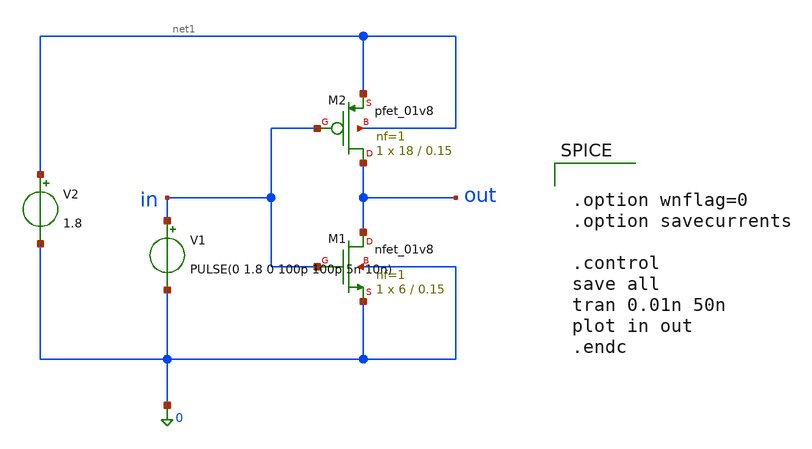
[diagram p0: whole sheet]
** sch_path: inverter_transient.sch
**.subckt inverter_transient
XM1 out in 0 0 sky130_fd_pr__nfet_01v8 L=0.15 W=6 nf=1 ad='int((1 + 1)/2) * 6 / 1 * 0.29' as='int((1 + 2)/2) * 6 / 1 * 0.29'
+ pd='2*int((1 + 1)/2) * (6 / 1 + 0.29)' ps='2*int((1 + 2)/2) * (6 / 1 + 0.29)' nrd='0.29 / 6 ' nrs='0.29 / 6 '
+ sa=0 sb=0 sd=0 mult=1 m=1
XM2 out in net1 net1 sky130_fd_pr__pfet_01v8 L=0.15 W=18 nf=1 ad='int((1 + 1)/2) * 18 / 1 * 0.29' as='int((1 + 2)/2) * 18 / 1 * 0.29'
+ pd='2*int((1 + 1)/2) * (18 / 1 + 0.29)' ps='2*int((1 + 2)/2) * (18 / 1 + 0.29)' nrd='0.29 / 18 ' nrs='0.29 / 18 '
+ sa=0 sb=0 sd=0 mult=1 m=1
V1 in 0 PULSE(0 1.8 0 100p 100p 5n 10n)
V2 net1 0 1.8
**** begin user architecture code

.lib /foss/pdks/sky130A/libs.tech/ngspice/sky130.lib.spice tt

.param mc_mm_switch=0
.param mc_pr_switch=1




.option wnflag=0
.option savecurrents

.control
save all
tran 0.01n 50n
plot in out
.endc


**** end user architecture code
**.ends
.end
